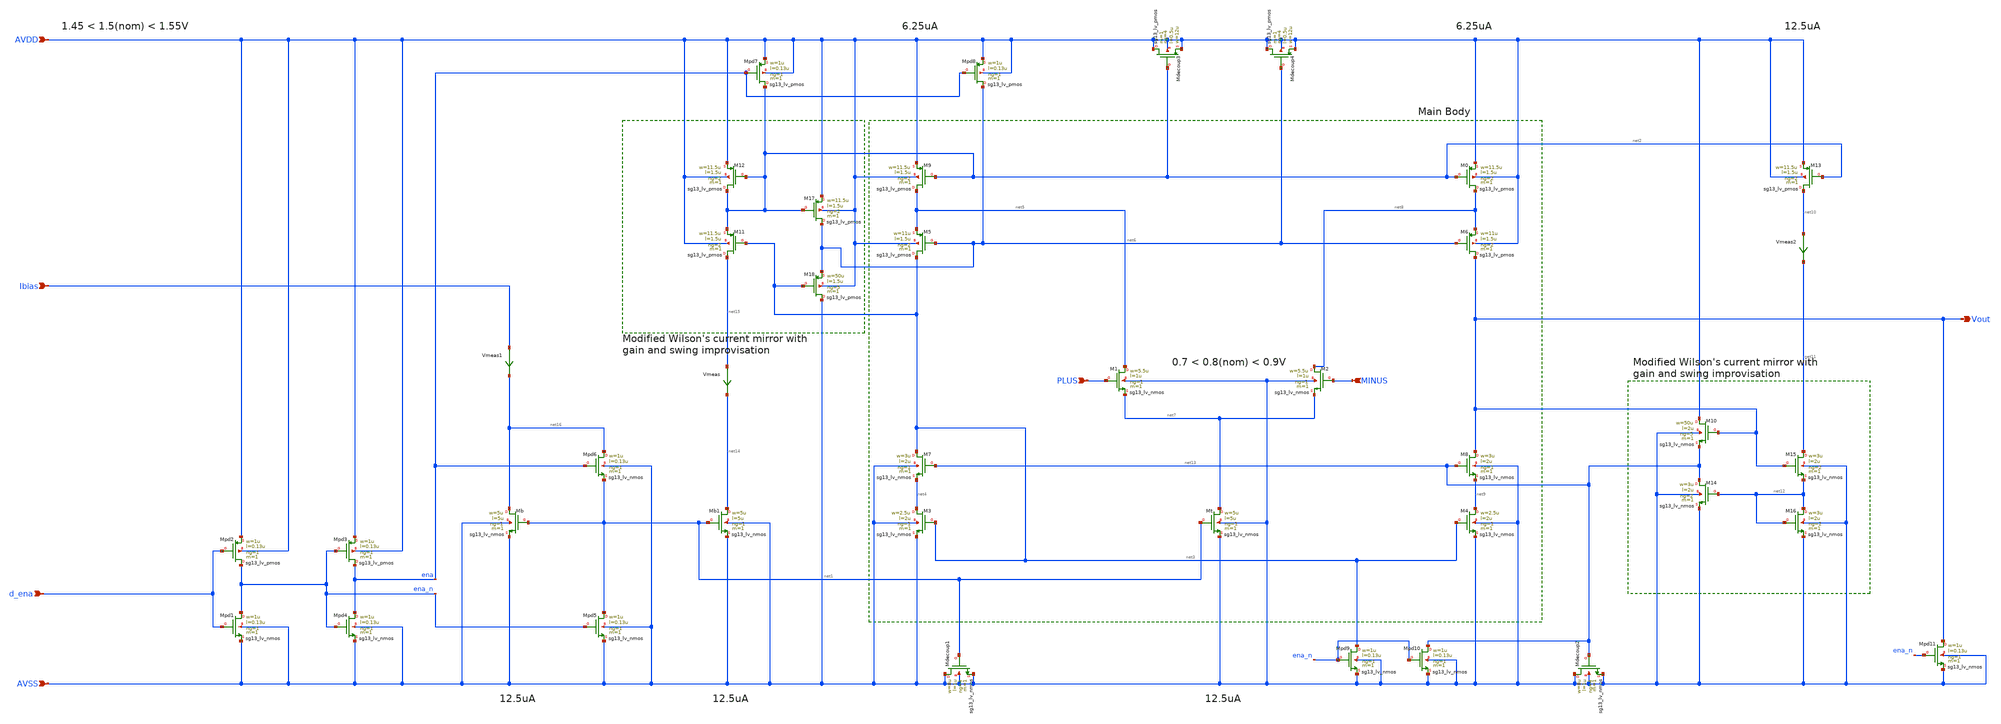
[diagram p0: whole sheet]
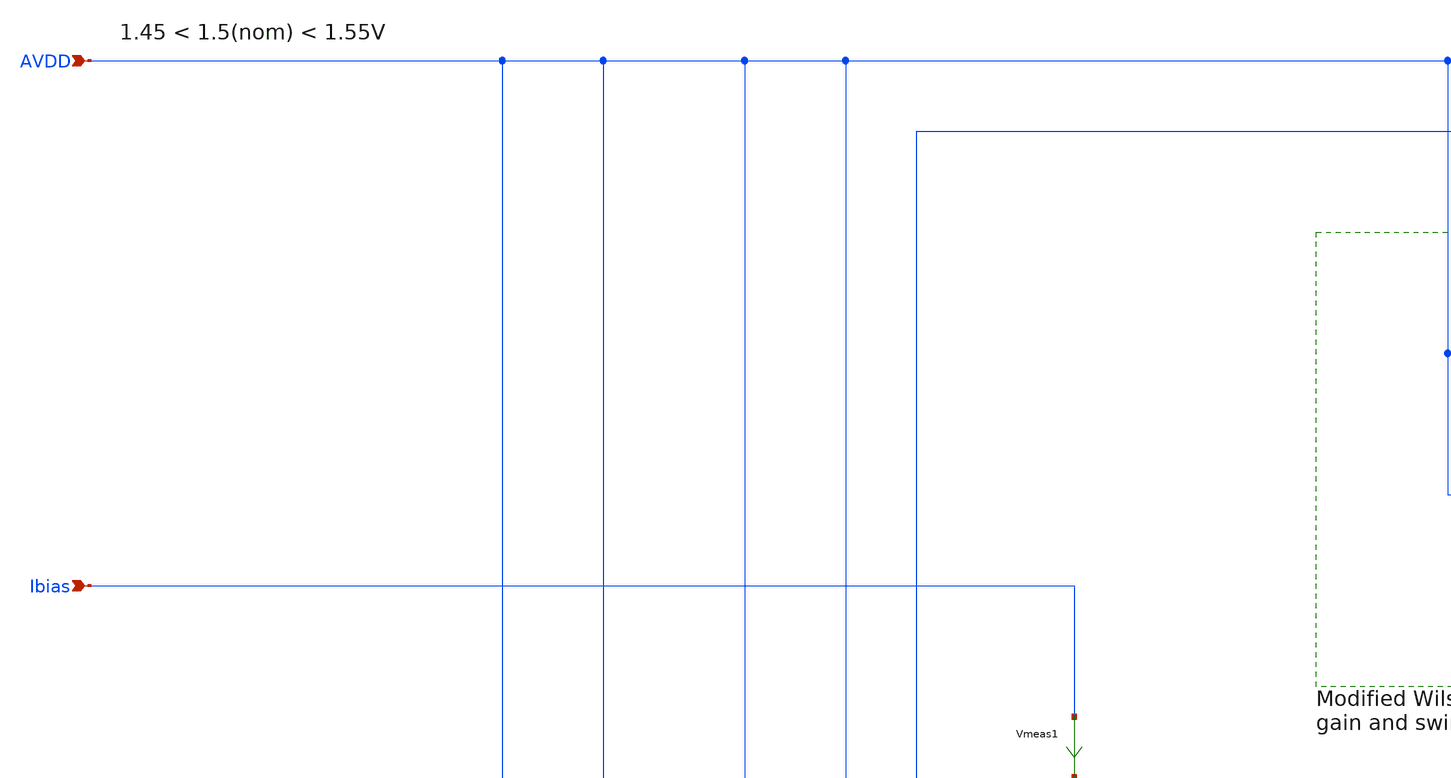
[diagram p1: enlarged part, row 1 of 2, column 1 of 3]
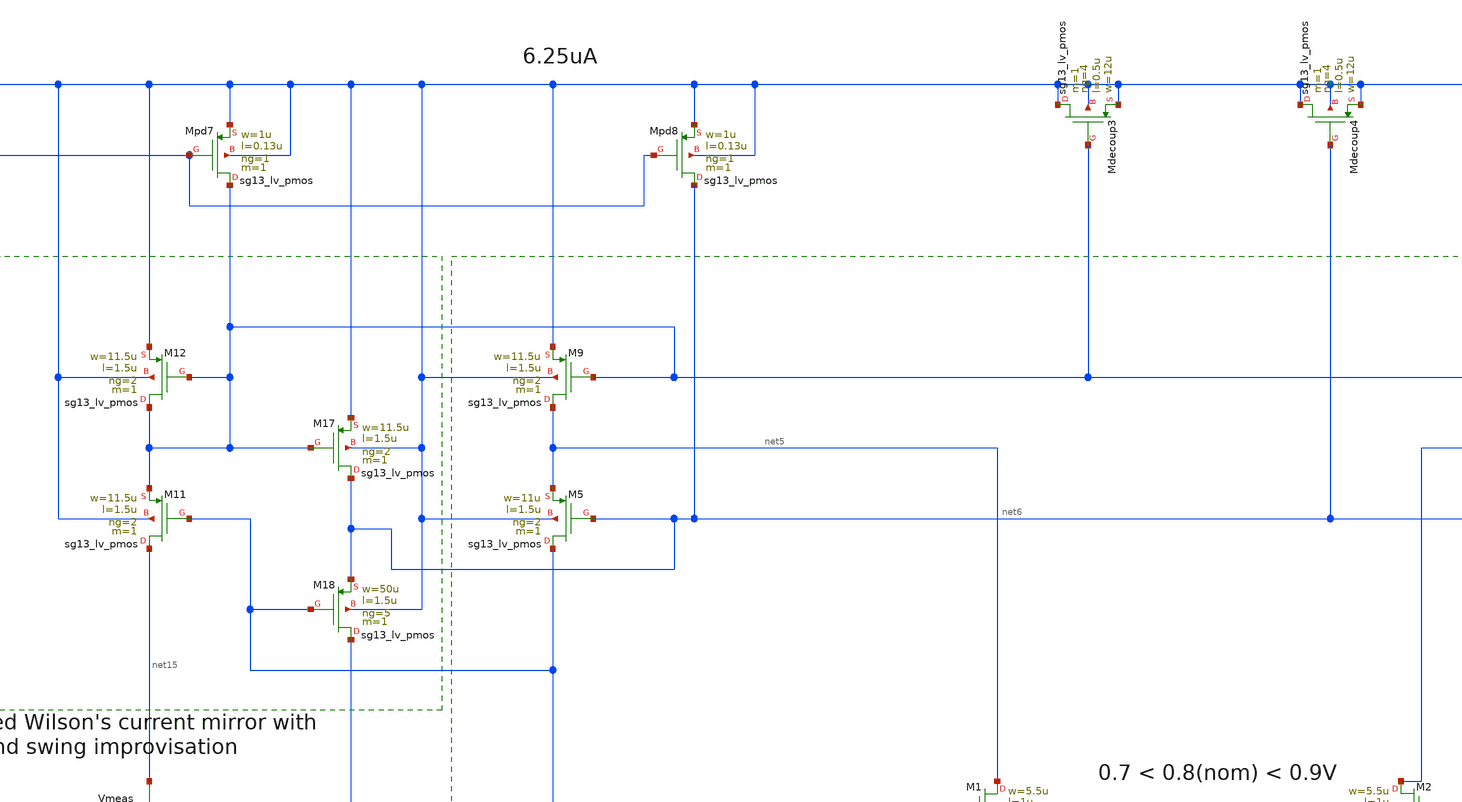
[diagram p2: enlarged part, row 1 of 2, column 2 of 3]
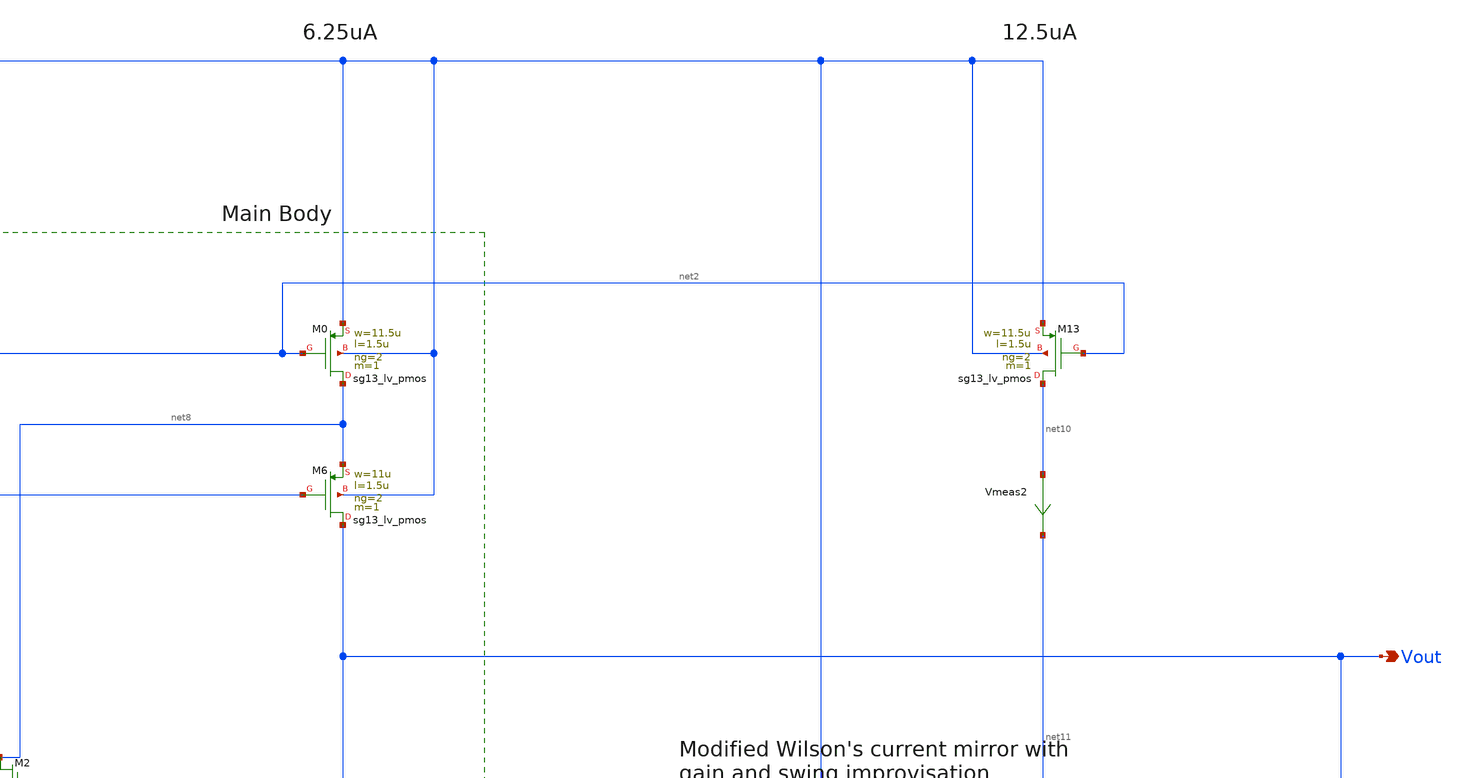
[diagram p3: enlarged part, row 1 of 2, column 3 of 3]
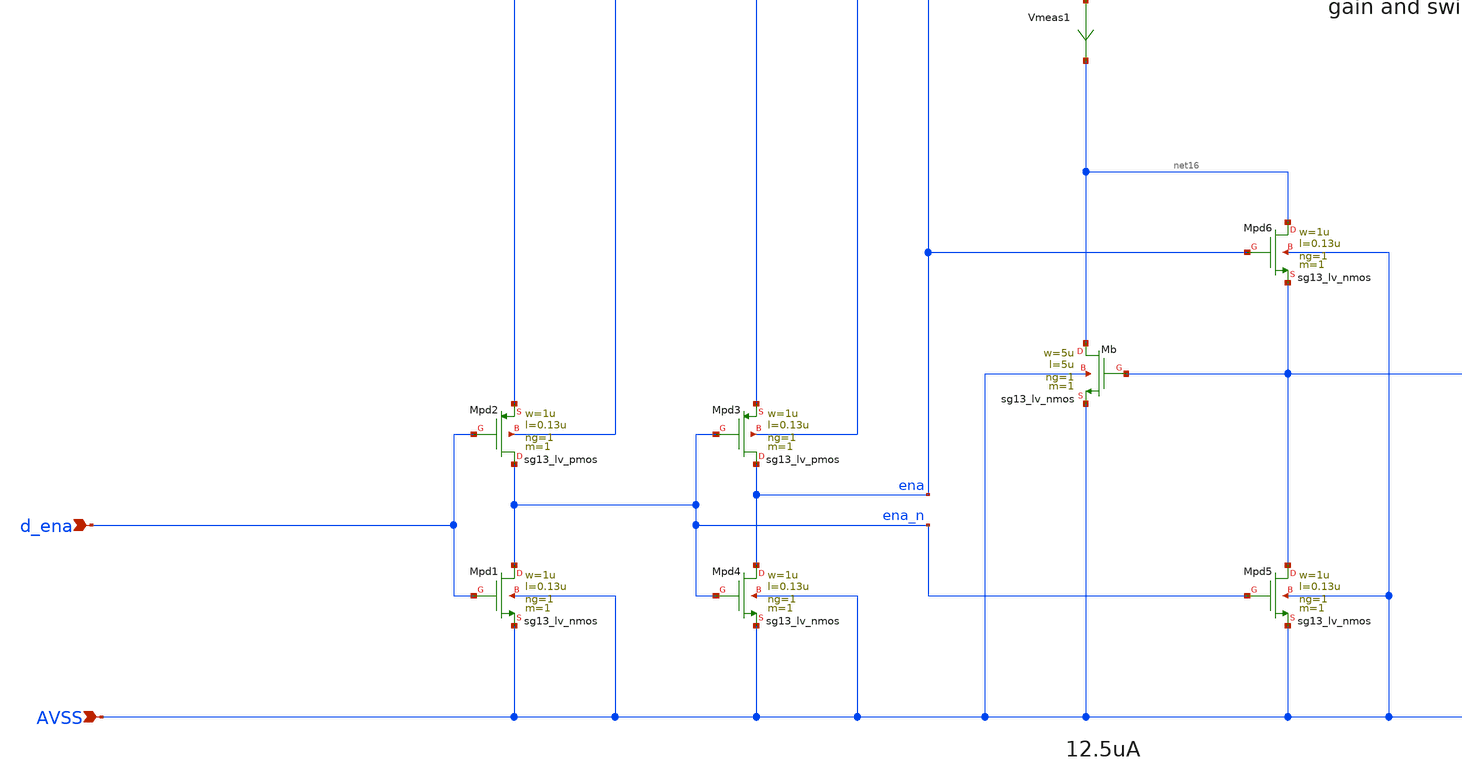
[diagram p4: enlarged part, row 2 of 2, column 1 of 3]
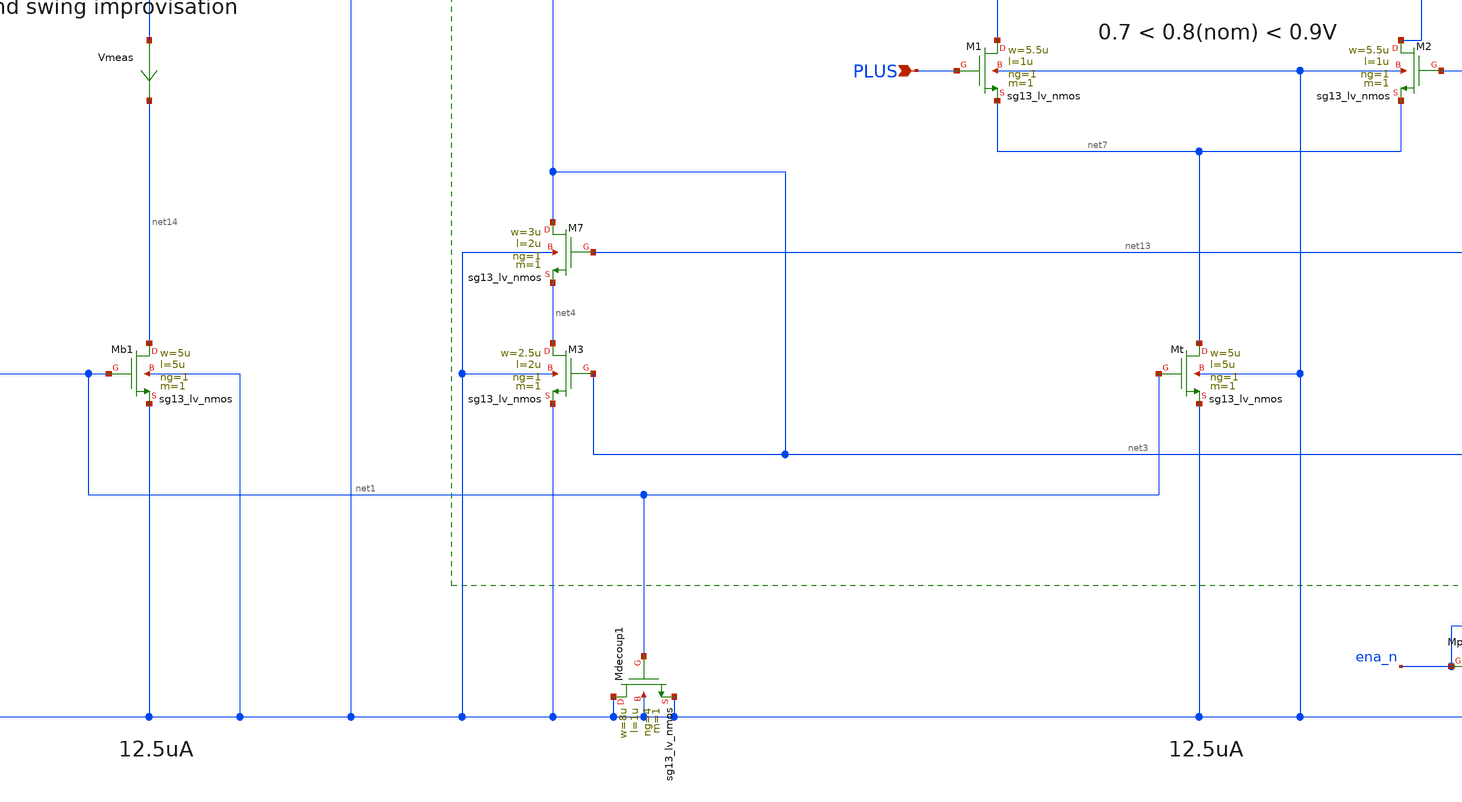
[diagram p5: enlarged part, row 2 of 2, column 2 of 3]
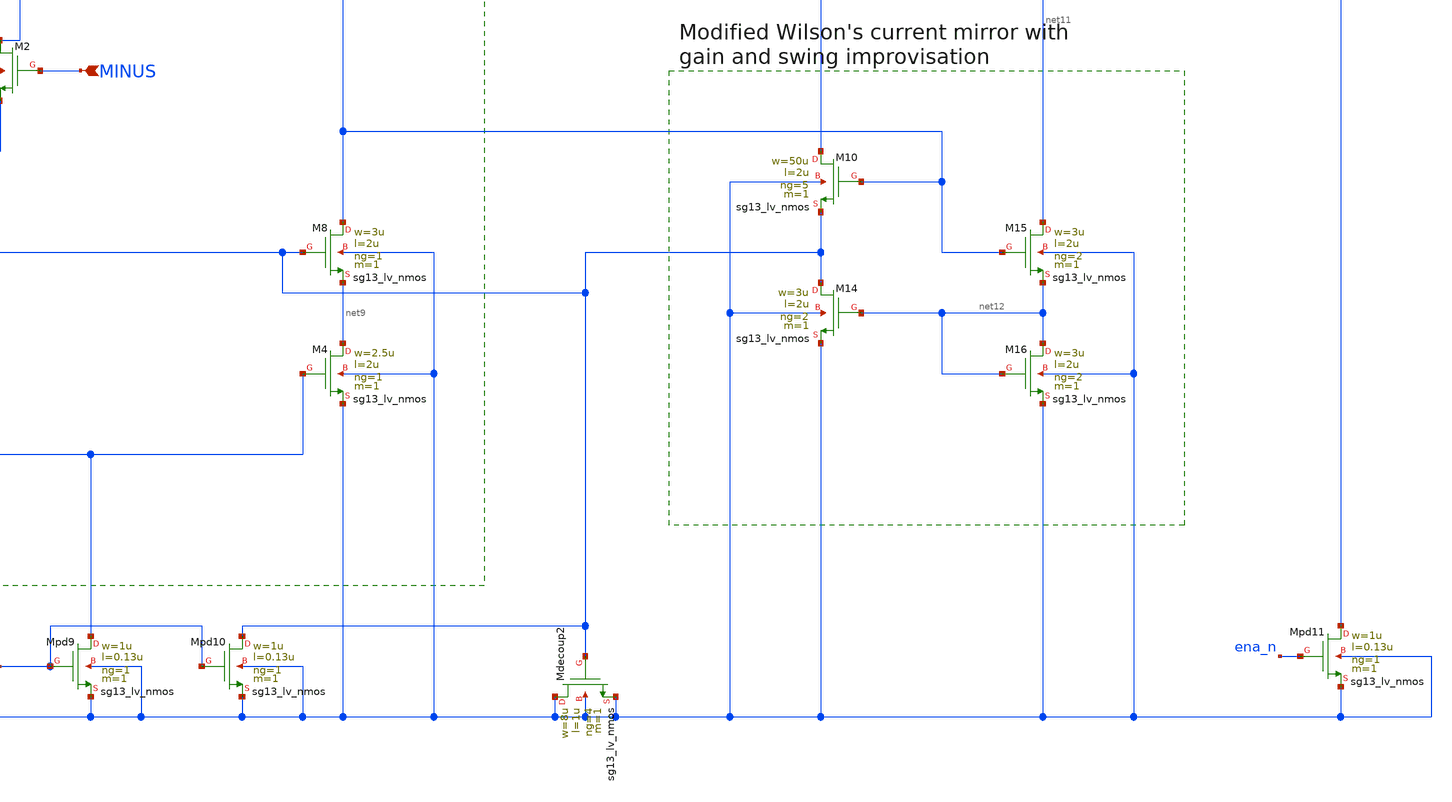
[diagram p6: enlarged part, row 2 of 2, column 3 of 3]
** sch_path: Designs/otas/1_schematics/foldedcascode_nmos_withdummies.sch
**.subckt foldedcascode_nmos_withdummies AVSS Ibias AVDD PLUS MINUS Vout d_ena
*.ipin AVSS
*.ipin Ibias
*.ipin AVDD
*.ipin PLUS
*.ipin MINUS
*.opin Vout
*.ipin d_ena
XMb net16 net1 AVSS AVSS sg13_lv_nmos w=5u l=5u ng=1 m=1 mm_ok=1
XMpd5 net1 ena_n AVSS AVSS sg13_lv_nmos w=1u l=0.13u ng=1 m=1 mm_ok=1
XMpd6 net16 ena net1 AVSS sg13_lv_nmos w=1u l=0.13u ng=1 m=1 mm_ok=1
XMb1 net14 net1 AVSS AVSS sg13_lv_nmos w=5u l=5u ng=1 m=1 mm_ok=1
Vmeas net15 net14 0
.save i(vmeas)
XM11 net15 net3 net2 AVDD sg13_lv_pmos w=11.5u l=1.5u ng=2 m=1 mm_ok=1
XM12 net2 net2 AVDD AVDD sg13_lv_pmos w=11.5u l=1.5u ng=2 m=1 mm_ok=1
XM18 AVSS net3 net6 AVDD sg13_lv_pmos w=50u l=1.5u ng=5 m=1 mm_ok=1
XM17 net6 net2 AVDD AVDD sg13_lv_pmos w=11.5u l=1.5u ng=2 m=1 mm_ok=1
XM9 net5 net2 AVDD AVDD sg13_lv_pmos w=11.5u l=1.5u ng=2 m=1 mm_ok=1
XM5 net3 net6 net5 AVDD sg13_lv_pmos w=11u l=1.5u ng=2 m=1 mm_ok=1
XM7 net3 net13 net4 AVSS sg13_lv_nmos w=3u l=2u ng=1 m=1 mm_ok=1
XM3 net4 net3 AVSS AVSS sg13_lv_nmos w=2.5u l=2u ng=1 m=1 mm_ok=1
XMpd7 net2 ena AVDD AVDD sg13_lv_pmos w=1u l=0.13u ng=1 m=1 mm_ok=1
XMpd8 net6 ena AVDD AVDD sg13_lv_pmos w=1u l=0.13u ng=1 m=1 mm_ok=1
XMt net7 net1 AVSS AVSS sg13_lv_nmos w=5u l=5u ng=1 m=1 mm_ok=1
XM1 net5 PLUS net7 AVSS sg13_lv_nmos w=5.5u l=1u ng=1 m=1 mm_ok=1
XM2 net8 MINUS net7 AVSS sg13_lv_nmos w=5.5u l=1u ng=1 m=1 mm_ok=1
XM6 Vout net6 net8 AVDD sg13_lv_pmos w=11u l=1.5u ng=2 m=1 mm_ok=1
XM0 net8 net2 AVDD AVDD sg13_lv_pmos w=11.5u l=1.5u ng=2 m=1 mm_ok=1
XMdecoup3 AVDD net2 AVDD AVDD sg13_lv_pmos w=12u l=0.5u ng=4 m=1 mm_ok=1
XMdecoup4 AVDD net6 AVDD AVDD sg13_lv_pmos w=12u l=0.5u ng=4 m=1 mm_ok=1
XM8 Vout net13 net9 AVSS sg13_lv_nmos w=3u l=2u ng=1 m=1 mm_ok=1
XM4 net9 net3 AVSS AVSS sg13_lv_nmos w=2.5u l=2u ng=1 m=1 mm_ok=1
XMdecoup1 AVSS net1 AVSS AVSS sg13_lv_nmos w=8u l=1u ng=4 m=1 mm_ok=1
XM13 net10 net2 AVDD AVDD sg13_lv_pmos w=11.5u l=1.5u ng=2 m=1 mm_ok=1
Vmeas2 net10 net11 0
.save i(vmeas2)
XM15 net11 Vout net12 AVSS sg13_lv_nmos w=3u l=2u ng=2 m=1 mm_ok=1
XM16 net12 net12 AVSS AVSS sg13_lv_nmos w=3u l=2u ng=2 m=1 mm_ok=1
XM14 net13 net12 AVSS AVSS sg13_lv_nmos w=3u l=2u ng=2 m=1 mm_ok=1
XM10 AVDD Vout net13 AVSS sg13_lv_nmos w=50u l=2u ng=5 m=1 mm_ok=1
XMpd11 Vout ena_n AVSS AVSS sg13_lv_nmos w=1u l=0.13u ng=1 m=1 mm_ok=1
XMdecoup2 AVSS net13 AVSS AVSS sg13_lv_nmos w=8u l=1u ng=4 m=1 mm_ok=1
XMpd10 net13 ena_n AVSS AVSS sg13_lv_nmos w=1u l=0.13u ng=1 m=1 mm_ok=1
XMpd9 net3 ena_n AVSS AVSS sg13_lv_nmos w=1u l=0.13u ng=1 m=1 mm_ok=1
XMpd2 ena_n d_ena AVDD AVDD sg13_lv_pmos w=1u l=0.13u ng=1 m=1 mm_ok=1
Vmeas1 Ibias net16 0
.save i(vmeas1)
XMpd3 ena ena_n AVDD AVDD sg13_lv_pmos w=1u l=0.13u ng=1 m=1 mm_ok=1
XMpd1 ena_n d_ena AVSS AVSS sg13_lv_nmos w=1u l=0.13u ng=1 m=1 mm_ok=1
XMpd4 ena ena_n AVSS AVSS sg13_lv_nmos w=1u l=0.13u ng=1 m=1 mm_ok=1
**.ends
.end
